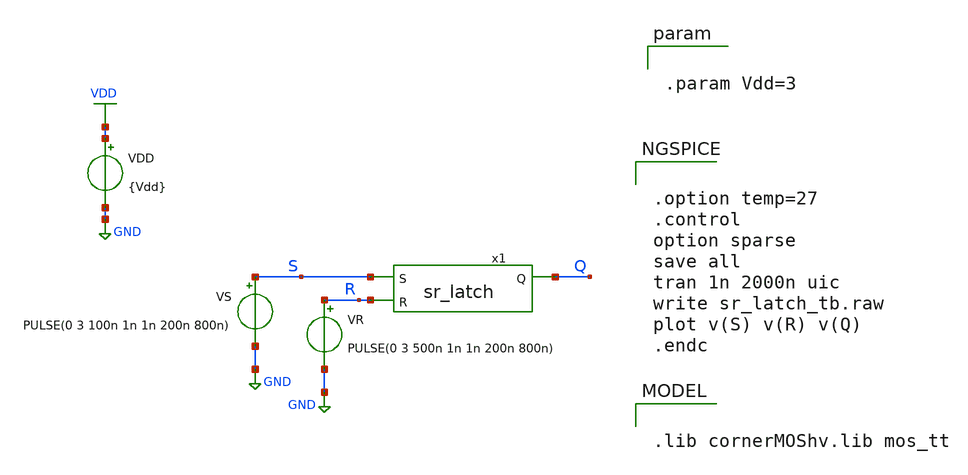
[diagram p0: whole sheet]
** sch_path: 3_real_circuits/sr_latch_tb.sch
**.subckt sr_latch_tb
x1 S Q R sr_latch
VDD VDD GND {Vdd}
VS S GND PULSE(0 3 100n 1n 1n 200n 800n)
VR R GND PULSE(0 3 500n 1n 1n 200n 800n)
**** begin user architecture code


.param Vdd=3




.option temp=27
.control
option sparse
save all
tran 1n 2000n uic
write sr_latch_tb.raw
plot v(S) v(R) v(Q)
.endc



.lib cornerMOShv.lib mos_tt

**** end user architecture code
**.ends

* expanding   symbol:  sr_latch.sym # of pins=3
** sym_path: 3_real_circuits/sr_latch.sym
** sch_path: 3_real_circuits/sr_latch.sch
.subckt sr_latch S Q R
*.ipin S
*.ipin R
*.opin Q
x2 R net3 inverter
x3 net1 net2 Q nand_gate
x1 S net1 inverter
x5 Q net3 net2 nand_gate
.ends


* expanding   symbol:  inverter.sym # of pins=2
** sym_path: 3_real_circuits/inverter.sym
** sch_path: 3_real_circuits/inverter.sch
.subckt inverter A Y
*.opin Y
*.ipin A
XM2 Y A GND GND sg13_hv_nmos w=0.3u l=0.45u ng=1 m=1 mm_ok=1
XM1 Y A VDD VDD sg13_hv_pmos w=0.3u l=0.4u ng=1 m=1 mm_ok=1
.ends


* expanding   symbol:  nand_gate.sym # of pins=3
** sym_path: 3_real_circuits/nand_gate.sym
** sch_path: 3_real_circuits/nand_gate.sch
.subckt nand_gate A B Y
*.ipin A
*.ipin B
*.opin Y
XM1 Y B VDD VDD sg13_hv_pmos w=0.3u l=0.4u ng=1 m=1 mm_ok=1
XM2 Y A VDD VDD sg13_hv_pmos w=0.3u l=0.4u ng=1 m=1 mm_ok=1
XM3 Y A net1 GND sg13_hv_nmos w=0.3u l=0.45u ng=1 m=1 mm_ok=1
XM4 net1 B GND GND sg13_hv_nmos w=0.3u l=0.45u ng=1 m=1 mm_ok=1
.ends

.GLOBAL VDD
.GLOBAL GND
.end
